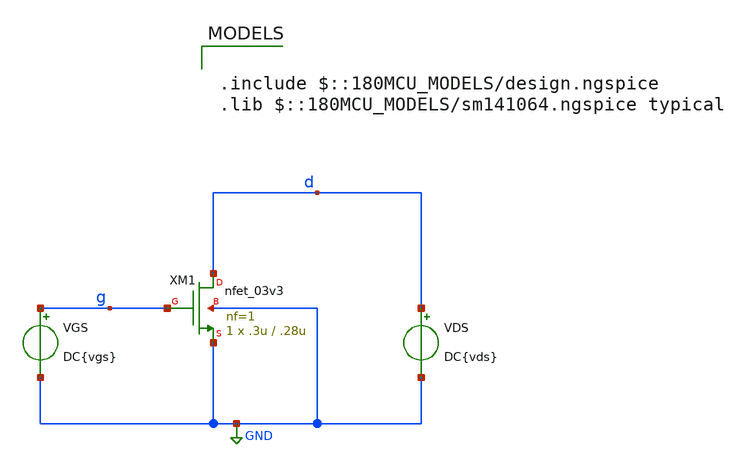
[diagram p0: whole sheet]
** sch_path: DAC_PAKISTAN_01/Pakistan1_Xschem/nmos_char_dc.sch
**.subckt nmos_char_dc
XM1 d g GND GND nfet_03v3 L=.28u W=.3u nf=1 ad='int((nf+1)/2) * W/nf * 0.18u' as='int((nf+2)/2) * W/nf * 0.18u'
+ pd='2*int((nf+1)/2) * (W/nf + 0.18u)' ps='2*int((nf+2)/2) * (W/nf + 0.18u)' nrd='0.18u / W' nrs='0.18u / W'
+ sa=0 sb=0 sd=0 m=1
VGS g GND DC{vgs}
VDS d GND DC{vds}
**** begin user architecture code



*Parameters
.param vds = 200m
.param vgs = 1.2

.options TEMP = 50.0

*Models

*Data to save
.save all  @M.xm1.m0[id]  @M.xm1.m0[vds]  @M.xm1.m0[vgs]  @M.xm1.m0[vth]  @M.xm1.m0[cgg]  @M.xm1.m0[cgs]  @M.xm1.m0[gds]  @M.xm1.m0[gm]  @M.xm1.m0[vdsat]

*Simulation
.control

dc VDS 0 3.3 0.01
setplot dc1
plot @M.xm1.m0[id] ylabel Id xlabel Vds
set filetype = binary
write nmos_char_dc_1.raw

reset
dc VGS 0 3.3 0.01
setplot dc2
plot @M.xm1.m0[id] ylabel Id xlabel Vgs
set filetype = binary
write nmos_char_dc_2.raw

reset
op
save all
set filetype = binary
write nmos_char_dc.raw

.endc
.end



.include $::180MCU_MODELS/design.ngspice
.lib $::180MCU_MODELS/sm141064.ngspice typical

**** end user architecture code
**.ends
.GLOBAL GND
.end
